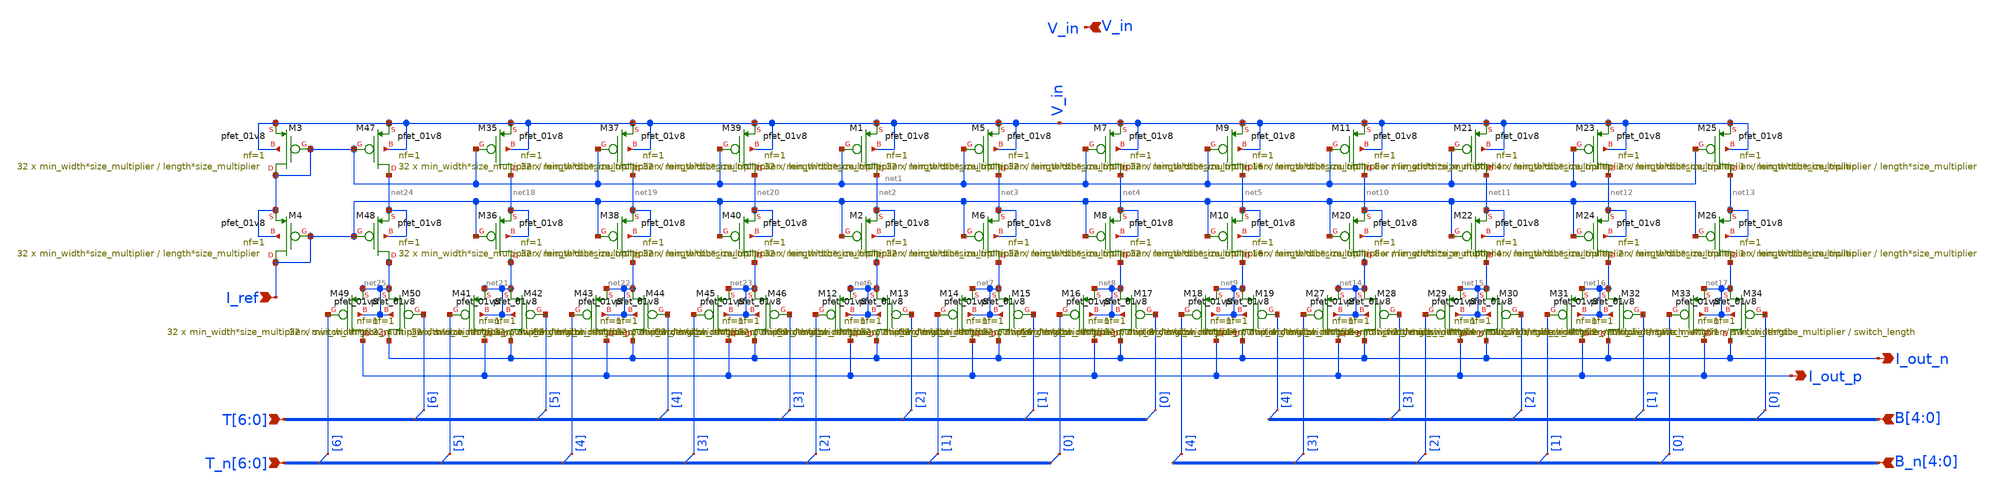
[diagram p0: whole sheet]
** sch_path: analog/schematics/components/DAC/segmented_dac.sch
**.subckt segmented_dac I_out_p V_in I_out_n I_ref B[4],B[3],B[2],B[1],B[0]
*+ B_n[4],B_n[3],B_n[2],B_n[1],B_n[0] T[6],T[5],T[4],T[3],T[2],T[1],T[0] T_n[6],T_n[5],T_n[4],T_n[3],T_n[2],T_n[1],T_n[0]
*.opin I_out_p
*.ipin V_in
*.opin I_out_n
*.ipin I_ref
*.ipin B[4],B[3],B[2],B[1],B[0]
*.ipin B_n[4],B_n[3],B_n[2],B_n[1],B_n[0]
*.ipin T[6],T[5],T[4],T[3],T[2],T[1],T[0]
*.ipin T_n[6],T_n[5],T_n[4],T_n[3],T_n[2],T_n[1],T_n[0]
XM1 net2 net1 V_in V_in sky130_fd_pr__pfet_01v8 L=length*size_multiplier W=min_width*size_multiplier
+ nf=1 ad='int((nf+1)/2) * W/nf * 0.29' as='int((nf+2)/2) * W/nf * 0.29' pd='2*int((nf+1)/2) * (W/nf + 0.29)'
+ ps='2*int((nf+2)/2) * (W/nf + 0.29)' nrd='0.29 / W' nrs='0.29 / W' sa=0 sb=0 sd=0 mult=32 m=32
XM2 net6 I_ref net2 net2 sky130_fd_pr__pfet_01v8 L=length*size_multiplier W=min_width*size_multiplier
+ nf=1 ad='int((nf+1)/2) * W/nf * 0.29' as='int((nf+2)/2) * W/nf * 0.29' pd='2*int((nf+1)/2) * (W/nf + 0.29)'
+ ps='2*int((nf+2)/2) * (W/nf + 0.29)' nrd='0.29 / W' nrs='0.29 / W' sa=0 sb=0 sd=0 mult=32 m=32
XM3 net1 net1 V_in V_in sky130_fd_pr__pfet_01v8 L=length*size_multiplier W=min_width*size_multiplier
+ nf=1 ad='int((nf+1)/2) * W/nf * 0.29' as='int((nf+2)/2) * W/nf * 0.29' pd='2*int((nf+1)/2) * (W/nf + 0.29)'
+ ps='2*int((nf+2)/2) * (W/nf + 0.29)' nrd='0.29 / W' nrs='0.29 / W' sa=0 sb=0 sd=0 mult=32 m=32
XM4 I_ref I_ref net1 net1 sky130_fd_pr__pfet_01v8 L=length*size_multiplier W=min_width*size_multiplier
+ nf=1 ad='int((nf+1)/2) * W/nf * 0.29' as='int((nf+2)/2) * W/nf * 0.29' pd='2*int((nf+1)/2) * (W/nf + 0.29)'
+ ps='2*int((nf+2)/2) * (W/nf + 0.29)' nrd='0.29 / W' nrs='0.29 / W' sa=0 sb=0 sd=0 mult=32 m=32
XM5 net3 net1 V_in V_in sky130_fd_pr__pfet_01v8 L=length*size_multiplier W=min_width*size_multiplier
+ nf=1 ad='int((nf+1)/2) * W/nf * 0.29' as='int((nf+2)/2) * W/nf * 0.29' pd='2*int((nf+1)/2) * (W/nf + 0.29)'
+ ps='2*int((nf+2)/2) * (W/nf + 0.29)' nrd='0.29 / W' nrs='0.29 / W' sa=0 sb=0 sd=0 mult=32 m=32
XM6 net7 I_ref net3 net3 sky130_fd_pr__pfet_01v8 L=length*size_multiplier W=min_width*size_multiplier
+ nf=1 ad='int((nf+1)/2) * W/nf * 0.29' as='int((nf+2)/2) * W/nf * 0.29' pd='2*int((nf+1)/2) * (W/nf + 0.29)'
+ ps='2*int((nf+2)/2) * (W/nf + 0.29)' nrd='0.29 / W' nrs='0.29 / W' sa=0 sb=0 sd=0 mult=32 m=32
XM7 net4 net1 V_in V_in sky130_fd_pr__pfet_01v8 L=length*size_multiplier W=min_width*size_multiplier
+ nf=1 ad='int((nf+1)/2) * W/nf * 0.29' as='int((nf+2)/2) * W/nf * 0.29' pd='2*int((nf+1)/2) * (W/nf + 0.29)'
+ ps='2*int((nf+2)/2) * (W/nf + 0.29)' nrd='0.29 / W' nrs='0.29 / W' sa=0 sb=0 sd=0 mult=32 m=32
XM8 net8 I_ref net4 net4 sky130_fd_pr__pfet_01v8 L=length*size_multiplier W=min_width*size_multiplier
+ nf=1 ad='int((nf+1)/2) * W/nf * 0.29' as='int((nf+2)/2) * W/nf * 0.29' pd='2*int((nf+1)/2) * (W/nf + 0.29)'
+ ps='2*int((nf+2)/2) * (W/nf + 0.29)' nrd='0.29 / W' nrs='0.29 / W' sa=0 sb=0 sd=0 mult=32 m=32
XM9 net5 net1 V_in V_in sky130_fd_pr__pfet_01v8 L=length*size_multiplier W=min_width*size_multiplier
+ nf=1 ad='int((nf+1)/2) * W/nf * 0.29' as='int((nf+2)/2) * W/nf * 0.29' pd='2*int((nf+1)/2) * (W/nf + 0.29)'
+ ps='2*int((nf+2)/2) * (W/nf + 0.29)' nrd='0.29 / W' nrs='0.29 / W' sa=0 sb=0 sd=0 mult=16 m=16
XM10 net9 I_ref net5 net5 sky130_fd_pr__pfet_01v8 L=length*size_multiplier W=min_width*size_multiplier
+ nf=1 ad='int((nf+1)/2) * W/nf * 0.29' as='int((nf+2)/2) * W/nf * 0.29' pd='2*int((nf+1)/2) * (W/nf + 0.29)'
+ ps='2*int((nf+2)/2) * (W/nf + 0.29)' nrd='0.29 / W' nrs='0.29 / W' sa=0 sb=0 sd=0 mult=16 m=16
XM12 I_out_p T_n[2] net6 net6 sky130_fd_pr__pfet_01v8 L=switch_length W=min_width*size_multiplier nf=1
+ ad='int((nf+1)/2) * W/nf * 0.29' as='int((nf+2)/2) * W/nf * 0.29' pd='2*int((nf+1)/2) * (W/nf + 0.29)'
+ ps='2*int((nf+2)/2) * (W/nf + 0.29)' nrd='0.29 / W' nrs='0.29 / W' sa=0 sb=0 sd=0 mult=32 m=32
XM13 I_out_n T[2] net6 net6 sky130_fd_pr__pfet_01v8 L=switch_length W=min_width*size_multiplier nf=1
+ ad='int((nf+1)/2) * W/nf * 0.29' as='int((nf+2)/2) * W/nf * 0.29' pd='2*int((nf+1)/2) * (W/nf + 0.29)'
+ ps='2*int((nf+2)/2) * (W/nf + 0.29)' nrd='0.29 / W' nrs='0.29 / W' sa=0 sb=0 sd=0 mult=32 m=32
XM14 I_out_p T_n[1] net7 net7 sky130_fd_pr__pfet_01v8 L=switch_length W=min_width*size_multiplier nf=1
+ ad='int((nf+1)/2) * W/nf * 0.29' as='int((nf+2)/2) * W/nf * 0.29' pd='2*int((nf+1)/2) * (W/nf + 0.29)'
+ ps='2*int((nf+2)/2) * (W/nf + 0.29)' nrd='0.29 / W' nrs='0.29 / W' sa=0 sb=0 sd=0 mult=32 m=32
XM15 I_out_n T[1] net7 net7 sky130_fd_pr__pfet_01v8 L=switch_length W=min_width*size_multiplier nf=1
+ ad='int((nf+1)/2) * W/nf * 0.29' as='int((nf+2)/2) * W/nf * 0.29' pd='2*int((nf+1)/2) * (W/nf + 0.29)'
+ ps='2*int((nf+2)/2) * (W/nf + 0.29)' nrd='0.29 / W' nrs='0.29 / W' sa=0 sb=0 sd=0 mult=32 m=32
XM16 I_out_p T_n[0] net8 net8 sky130_fd_pr__pfet_01v8 L=switch_length W=min_width*size_multiplier nf=1
+ ad='int((nf+1)/2) * W/nf * 0.29' as='int((nf+2)/2) * W/nf * 0.29' pd='2*int((nf+1)/2) * (W/nf + 0.29)'
+ ps='2*int((nf+2)/2) * (W/nf + 0.29)' nrd='0.29 / W' nrs='0.29 / W' sa=0 sb=0 sd=0 mult=32 m=32
XM17 I_out_n T[0] net8 net8 sky130_fd_pr__pfet_01v8 L=switch_length W=min_width*size_multiplier nf=1
+ ad='int((nf+1)/2) * W/nf * 0.29' as='int((nf+2)/2) * W/nf * 0.29' pd='2*int((nf+1)/2) * (W/nf + 0.29)'
+ ps='2*int((nf+2)/2) * (W/nf + 0.29)' nrd='0.29 / W' nrs='0.29 / W' sa=0 sb=0 sd=0 mult=32 m=32
XM18 I_out_p B_n[4] net9 net9 sky130_fd_pr__pfet_01v8 L=switch_length W=min_width*size_multiplier nf=1
+ ad='int((nf+1)/2) * W/nf * 0.29' as='int((nf+2)/2) * W/nf * 0.29' pd='2*int((nf+1)/2) * (W/nf + 0.29)'
+ ps='2*int((nf+2)/2) * (W/nf + 0.29)' nrd='0.29 / W' nrs='0.29 / W' sa=0 sb=0 sd=0 mult=16 m=16
XM19 I_out_n B[4] net9 net9 sky130_fd_pr__pfet_01v8 L=switch_length W=min_width*size_multiplier nf=1
+ ad='int((nf+1)/2) * W/nf * 0.29' as='int((nf+2)/2) * W/nf * 0.29' pd='2*int((nf+1)/2) * (W/nf + 0.29)'
+ ps='2*int((nf+2)/2) * (W/nf + 0.29)' nrd='0.29 / W' nrs='0.29 / W' sa=0 sb=0 sd=0 mult=16 m=16
XM11 net10 net1 V_in V_in sky130_fd_pr__pfet_01v8 L=length*size_multiplier W=min_width*size_multiplier
+ nf=1 ad='int((nf+1)/2) * W/nf * 0.29' as='int((nf+2)/2) * W/nf * 0.29' pd='2*int((nf+1)/2) * (W/nf + 0.29)'
+ ps='2*int((nf+2)/2) * (W/nf + 0.29)' nrd='0.29 / W' nrs='0.29 / W' sa=0 sb=0 sd=0 mult=8 m=8
XM20 net14 I_ref net10 net10 sky130_fd_pr__pfet_01v8 L=length*size_multiplier W=min_width*size_multiplier
+ nf=1 ad='int((nf+1)/2) * W/nf * 0.29' as='int((nf+2)/2) * W/nf * 0.29' pd='2*int((nf+1)/2) * (W/nf + 0.29)'
+ ps='2*int((nf+2)/2) * (W/nf + 0.29)' nrd='0.29 / W' nrs='0.29 / W' sa=0 sb=0 sd=0 mult=8 m=8
XM21 net11 net1 V_in V_in sky130_fd_pr__pfet_01v8 L=length*size_multiplier W=min_width*size_multiplier
+ nf=1 ad='int((nf+1)/2) * W/nf * 0.29' as='int((nf+2)/2) * W/nf * 0.29' pd='2*int((nf+1)/2) * (W/nf + 0.29)'
+ ps='2*int((nf+2)/2) * (W/nf + 0.29)' nrd='0.29 / W' nrs='0.29 / W' sa=0 sb=0 sd=0 mult=4 m=4
XM22 net15 I_ref net11 net11 sky130_fd_pr__pfet_01v8 L=length*size_multiplier W=min_width*size_multiplier
+ nf=1 ad='int((nf+1)/2) * W/nf * 0.29' as='int((nf+2)/2) * W/nf * 0.29' pd='2*int((nf+1)/2) * (W/nf + 0.29)'
+ ps='2*int((nf+2)/2) * (W/nf + 0.29)' nrd='0.29 / W' nrs='0.29 / W' sa=0 sb=0 sd=0 mult=4 m=4
XM23 net12 net1 V_in V_in sky130_fd_pr__pfet_01v8 L=length*size_multiplier W=min_width*size_multiplier
+ nf=1 ad='int((nf+1)/2) * W/nf * 0.29' as='int((nf+2)/2) * W/nf * 0.29' pd='2*int((nf+1)/2) * (W/nf + 0.29)'
+ ps='2*int((nf+2)/2) * (W/nf + 0.29)' nrd='0.29 / W' nrs='0.29 / W' sa=0 sb=0 sd=0 mult=2 m=2
XM24 net16 I_ref net12 net12 sky130_fd_pr__pfet_01v8 L=length*size_multiplier W=min_width*size_multiplier
+ nf=1 ad='int((nf+1)/2) * W/nf * 0.29' as='int((nf+2)/2) * W/nf * 0.29' pd='2*int((nf+1)/2) * (W/nf + 0.29)'
+ ps='2*int((nf+2)/2) * (W/nf + 0.29)' nrd='0.29 / W' nrs='0.29 / W' sa=0 sb=0 sd=0 mult=2 m=2
XM25 net13 net1 V_in V_in sky130_fd_pr__pfet_01v8 L=length*size_multiplier W=min_width*size_multiplier
+ nf=1 ad='int((nf+1)/2) * W/nf * 0.29' as='int((nf+2)/2) * W/nf * 0.29' pd='2*int((nf+1)/2) * (W/nf + 0.29)'
+ ps='2*int((nf+2)/2) * (W/nf + 0.29)' nrd='0.29 / W' nrs='0.29 / W' sa=0 sb=0 sd=0 mult=1 m=1
XM26 net17 I_ref net13 net13 sky130_fd_pr__pfet_01v8 L=length*size_multiplier W=min_width*size_multiplier
+ nf=1 ad='int((nf+1)/2) * W/nf * 0.29' as='int((nf+2)/2) * W/nf * 0.29' pd='2*int((nf+1)/2) * (W/nf + 0.29)'
+ ps='2*int((nf+2)/2) * (W/nf + 0.29)' nrd='0.29 / W' nrs='0.29 / W' sa=0 sb=0 sd=0 mult=1 m=1
XM27 I_out_p B_n[3] net14 net14 sky130_fd_pr__pfet_01v8 L=switch_length W=min_width*size_multiplier nf=1
+ ad='int((nf+1)/2) * W/nf * 0.29' as='int((nf+2)/2) * W/nf * 0.29' pd='2*int((nf+1)/2) * (W/nf + 0.29)'
+ ps='2*int((nf+2)/2) * (W/nf + 0.29)' nrd='0.29 / W' nrs='0.29 / W' sa=0 sb=0 sd=0 mult=8 m=8
XM28 I_out_n B[3] net14 net14 sky130_fd_pr__pfet_01v8 L=switch_length W=min_width*size_multiplier nf=1
+ ad='int((nf+1)/2) * W/nf * 0.29' as='int((nf+2)/2) * W/nf * 0.29' pd='2*int((nf+1)/2) * (W/nf + 0.29)'
+ ps='2*int((nf+2)/2) * (W/nf + 0.29)' nrd='0.29 / W' nrs='0.29 / W' sa=0 sb=0 sd=0 mult=8 m=8
XM29 I_out_p B_n[2] net15 net15 sky130_fd_pr__pfet_01v8 L=switch_length W=min_width*size_multiplier nf=1
+ ad='int((nf+1)/2) * W/nf * 0.29' as='int((nf+2)/2) * W/nf * 0.29' pd='2*int((nf+1)/2) * (W/nf + 0.29)'
+ ps='2*int((nf+2)/2) * (W/nf + 0.29)' nrd='0.29 / W' nrs='0.29 / W' sa=0 sb=0 sd=0 mult=4 m=4
XM30 I_out_n B[2] net15 net15 sky130_fd_pr__pfet_01v8 L=switch_length W=min_width*size_multiplier nf=1
+ ad='int((nf+1)/2) * W/nf * 0.29' as='int((nf+2)/2) * W/nf * 0.29' pd='2*int((nf+1)/2) * (W/nf + 0.29)'
+ ps='2*int((nf+2)/2) * (W/nf + 0.29)' nrd='0.29 / W' nrs='0.29 / W' sa=0 sb=0 sd=0 mult=4 m=4
XM31 I_out_p B_n[1] net16 net16 sky130_fd_pr__pfet_01v8 L=switch_length W=min_width*size_multiplier nf=1
+ ad='int((nf+1)/2) * W/nf * 0.29' as='int((nf+2)/2) * W/nf * 0.29' pd='2*int((nf+1)/2) * (W/nf + 0.29)'
+ ps='2*int((nf+2)/2) * (W/nf + 0.29)' nrd='0.29 / W' nrs='0.29 / W' sa=0 sb=0 sd=0 mult=2 m=2
XM32 I_out_n B[1] net16 net16 sky130_fd_pr__pfet_01v8 L=switch_length W=min_width*size_multiplier nf=1
+ ad='int((nf+1)/2) * W/nf * 0.29' as='int((nf+2)/2) * W/nf * 0.29' pd='2*int((nf+1)/2) * (W/nf + 0.29)'
+ ps='2*int((nf+2)/2) * (W/nf + 0.29)' nrd='0.29 / W' nrs='0.29 / W' sa=0 sb=0 sd=0 mult=2 m=2
XM33 I_out_p B_n[0] net17 net17 sky130_fd_pr__pfet_01v8 L=switch_length W=min_width*size_multiplier nf=1
+ ad='int((nf+1)/2) * W/nf * 0.29' as='int((nf+2)/2) * W/nf * 0.29' pd='2*int((nf+1)/2) * (W/nf + 0.29)'
+ ps='2*int((nf+2)/2) * (W/nf + 0.29)' nrd='0.29 / W' nrs='0.29 / W' sa=0 sb=0 sd=0 mult=1 m=1
XM34 I_out_n B[0] net17 net17 sky130_fd_pr__pfet_01v8 L=switch_length W=min_width*size_multiplier nf=1
+ ad='int((nf+1)/2) * W/nf * 0.29' as='int((nf+2)/2) * W/nf * 0.29' pd='2*int((nf+1)/2) * (W/nf + 0.29)'
+ ps='2*int((nf+2)/2) * (W/nf + 0.29)' nrd='0.29 / W' nrs='0.29 / W' sa=0 sb=0 sd=0 mult=1 m=1
XM35 net18 net1 V_in V_in sky130_fd_pr__pfet_01v8 L=length*size_multiplier W=min_width*size_multiplier
+ nf=1 ad='int((nf+1)/2) * W/nf * 0.29' as='int((nf+2)/2) * W/nf * 0.29' pd='2*int((nf+1)/2) * (W/nf + 0.29)'
+ ps='2*int((nf+2)/2) * (W/nf + 0.29)' nrd='0.29 / W' nrs='0.29 / W' sa=0 sb=0 sd=0 mult=32 m=32
XM36 net21 I_ref net18 net18 sky130_fd_pr__pfet_01v8 L=length*size_multiplier W=min_width*size_multiplier
+ nf=1 ad='int((nf+1)/2) * W/nf * 0.29' as='int((nf+2)/2) * W/nf * 0.29' pd='2*int((nf+1)/2) * (W/nf + 0.29)'
+ ps='2*int((nf+2)/2) * (W/nf + 0.29)' nrd='0.29 / W' nrs='0.29 / W' sa=0 sb=0 sd=0 mult=32 m=32
XM37 net19 net1 V_in V_in sky130_fd_pr__pfet_01v8 L=length*size_multiplier W=min_width*size_multiplier
+ nf=1 ad='int((nf+1)/2) * W/nf * 0.29' as='int((nf+2)/2) * W/nf * 0.29' pd='2*int((nf+1)/2) * (W/nf + 0.29)'
+ ps='2*int((nf+2)/2) * (W/nf + 0.29)' nrd='0.29 / W' nrs='0.29 / W' sa=0 sb=0 sd=0 mult=32 m=32
XM38 net22 I_ref net19 net19 sky130_fd_pr__pfet_01v8 L=length*size_multiplier W=min_width*size_multiplier
+ nf=1 ad='int((nf+1)/2) * W/nf * 0.29' as='int((nf+2)/2) * W/nf * 0.29' pd='2*int((nf+1)/2) * (W/nf + 0.29)'
+ ps='2*int((nf+2)/2) * (W/nf + 0.29)' nrd='0.29 / W' nrs='0.29 / W' sa=0 sb=0 sd=0 mult=32 m=32
XM39 net20 net1 V_in V_in sky130_fd_pr__pfet_01v8 L=length*size_multiplier W=min_width*size_multiplier
+ nf=1 ad='int((nf+1)/2) * W/nf * 0.29' as='int((nf+2)/2) * W/nf * 0.29' pd='2*int((nf+1)/2) * (W/nf + 0.29)'
+ ps='2*int((nf+2)/2) * (W/nf + 0.29)' nrd='0.29 / W' nrs='0.29 / W' sa=0 sb=0 sd=0 mult=32 m=32
XM40 net23 I_ref net20 net20 sky130_fd_pr__pfet_01v8 L=length*size_multiplier W=min_width*size_multiplier
+ nf=1 ad='int((nf+1)/2) * W/nf * 0.29' as='int((nf+2)/2) * W/nf * 0.29' pd='2*int((nf+1)/2) * (W/nf + 0.29)'
+ ps='2*int((nf+2)/2) * (W/nf + 0.29)' nrd='0.29 / W' nrs='0.29 / W' sa=0 sb=0 sd=0 mult=32 m=32
XM41 I_out_p T_n[5] net21 net21 sky130_fd_pr__pfet_01v8 L=switch_length W=min_width*size_multiplier nf=1
+ ad='int((nf+1)/2) * W/nf * 0.29' as='int((nf+2)/2) * W/nf * 0.29' pd='2*int((nf+1)/2) * (W/nf + 0.29)'
+ ps='2*int((nf+2)/2) * (W/nf + 0.29)' nrd='0.29 / W' nrs='0.29 / W' sa=0 sb=0 sd=0 mult=32 m=32
XM42 I_out_n T[5] net21 net21 sky130_fd_pr__pfet_01v8 L=switch_length W=min_width*size_multiplier nf=1
+ ad='int((nf+1)/2) * W/nf * 0.29' as='int((nf+2)/2) * W/nf * 0.29' pd='2*int((nf+1)/2) * (W/nf + 0.29)'
+ ps='2*int((nf+2)/2) * (W/nf + 0.29)' nrd='0.29 / W' nrs='0.29 / W' sa=0 sb=0 sd=0 mult=32 m=32
XM43 I_out_p T_n[4] net22 net22 sky130_fd_pr__pfet_01v8 L=switch_length W=min_width*size_multiplier nf=1
+ ad='int((nf+1)/2) * W/nf * 0.29' as='int((nf+2)/2) * W/nf * 0.29' pd='2*int((nf+1)/2) * (W/nf + 0.29)'
+ ps='2*int((nf+2)/2) * (W/nf + 0.29)' nrd='0.29 / W' nrs='0.29 / W' sa=0 sb=0 sd=0 mult=32 m=32
XM44 I_out_n T[4] net22 net22 sky130_fd_pr__pfet_01v8 L=switch_length W=min_width*size_multiplier nf=1
+ ad='int((nf+1)/2) * W/nf * 0.29' as='int((nf+2)/2) * W/nf * 0.29' pd='2*int((nf+1)/2) * (W/nf + 0.29)'
+ ps='2*int((nf+2)/2) * (W/nf + 0.29)' nrd='0.29 / W' nrs='0.29 / W' sa=0 sb=0 sd=0 mult=32 m=32
XM45 I_out_p T_n[3] net23 net23 sky130_fd_pr__pfet_01v8 L=switch_length W=min_width*size_multiplier nf=1
+ ad='int((nf+1)/2) * W/nf * 0.29' as='int((nf+2)/2) * W/nf * 0.29' pd='2*int((nf+1)/2) * (W/nf + 0.29)'
+ ps='2*int((nf+2)/2) * (W/nf + 0.29)' nrd='0.29 / W' nrs='0.29 / W' sa=0 sb=0 sd=0 mult=32 m=32
XM46 I_out_n T[3] net23 net23 sky130_fd_pr__pfet_01v8 L=switch_length W=min_width*size_multiplier nf=1
+ ad='int((nf+1)/2) * W/nf * 0.29' as='int((nf+2)/2) * W/nf * 0.29' pd='2*int((nf+1)/2) * (W/nf + 0.29)'
+ ps='2*int((nf+2)/2) * (W/nf + 0.29)' nrd='0.29 / W' nrs='0.29 / W' sa=0 sb=0 sd=0 mult=32 m=32
XM47 net24 net1 V_in V_in sky130_fd_pr__pfet_01v8 L=length*size_multiplier W=min_width*size_multiplier
+ nf=1 ad='int((nf+1)/2) * W/nf * 0.29' as='int((nf+2)/2) * W/nf * 0.29' pd='2*int((nf+1)/2) * (W/nf + 0.29)'
+ ps='2*int((nf+2)/2) * (W/nf + 0.29)' nrd='0.29 / W' nrs='0.29 / W' sa=0 sb=0 sd=0 mult=32 m=32
XM48 net25 I_ref net24 net24 sky130_fd_pr__pfet_01v8 L=length*size_multiplier W=min_width*size_multiplier
+ nf=1 ad='int((nf+1)/2) * W/nf * 0.29' as='int((nf+2)/2) * W/nf * 0.29' pd='2*int((nf+1)/2) * (W/nf + 0.29)'
+ ps='2*int((nf+2)/2) * (W/nf + 0.29)' nrd='0.29 / W' nrs='0.29 / W' sa=0 sb=0 sd=0 mult=32 m=32
XM49 I_out_p T_n[6] net25 net25 sky130_fd_pr__pfet_01v8 L=switch_length W=min_width*size_multiplier nf=1
+ ad='int((nf+1)/2) * W/nf * 0.29' as='int((nf+2)/2) * W/nf * 0.29' pd='2*int((nf+1)/2) * (W/nf + 0.29)'
+ ps='2*int((nf+2)/2) * (W/nf + 0.29)' nrd='0.29 / W' nrs='0.29 / W' sa=0 sb=0 sd=0 mult=32 m=32
XM50 I_out_n T[6] net25 net25 sky130_fd_pr__pfet_01v8 L=switch_length W=min_width*size_multiplier nf=1
+ ad='int((nf+1)/2) * W/nf * 0.29' as='int((nf+2)/2) * W/nf * 0.29' pd='2*int((nf+1)/2) * (W/nf + 0.29)'
+ ps='2*int((nf+2)/2) * (W/nf + 0.29)' nrd='0.29 / W' nrs='0.29 / W' sa=0 sb=0 sd=0 mult=32 m=32
* tap: B[4:0] --> B[0]
* tap: B[4:0] --> B[1]
* tap: B[4:0] --> B[2]
* tap: B[4:0] --> B[3]
* tap: B[4:0] --> B[4]
* tap: B_n[4:0] --> B_n[0]
* tap: B_n[4:0] --> B_n[1]
* tap: B_n[4:0] --> B_n[2]
* tap: B_n[4:0] --> B_n[3]
* tap: B_n[4:0] --> B_n[4]
* tap: T[6:0] --> T[0]
* tap: T[6:0] --> T[1]
* tap: T[6:0] --> T[2]
* tap: T[6:0] --> T[3]
* tap: T[6:0] --> T[4]
* tap: T[6:0] --> T[5]
* tap: T[6:0] --> T[6]
* tap: T_n[6:0] --> T_n[0]
* tap: T_n[6:0] --> T_n[1]
* tap: T_n[6:0] --> T_n[2]
* tap: T_n[6:0] --> T_n[3]
* tap: T_n[6:0] --> T_n[4]
* tap: T_n[6:0] --> T_n[5]
* tap: T_n[6:0] --> T_n[6]
**.ends
.end
